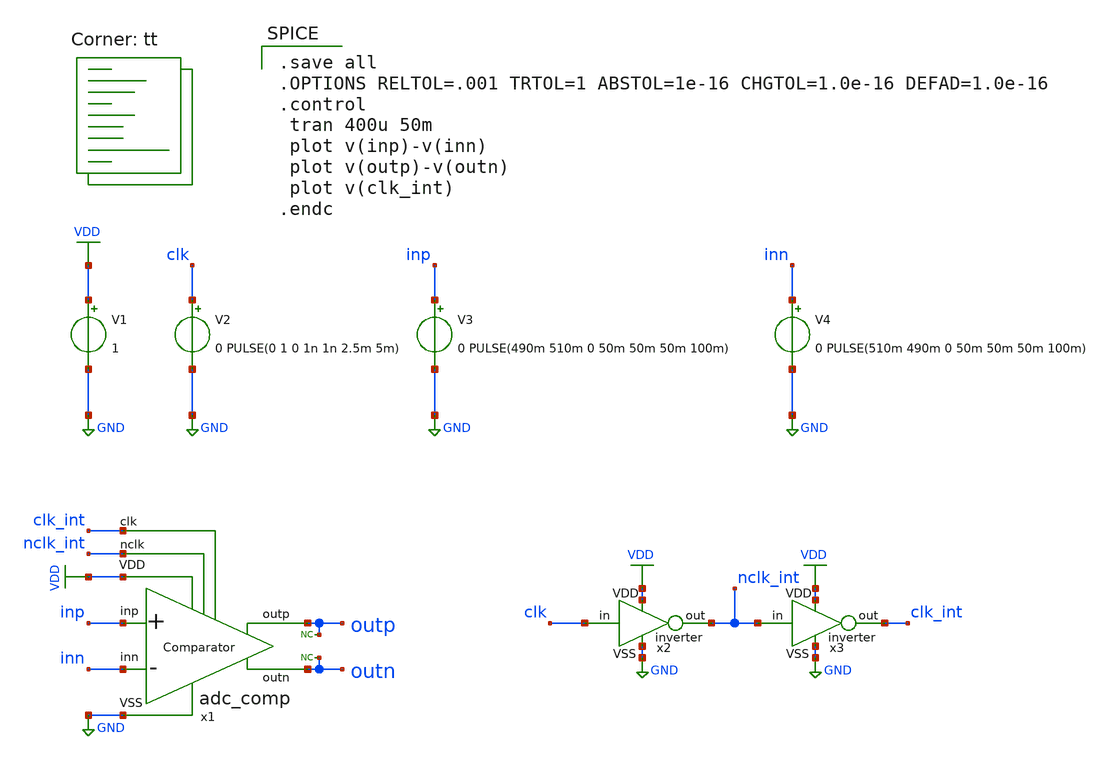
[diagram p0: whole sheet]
** sch_path: xschem/adc_comp/adc_comp_tb.sch
**.subckt adc_comp_tb
x1 VDD clk_int outp inp inn outn nclk_int GND adc_comp
V1 VDD GND 1
V2 clk GND 0 PULSE(0 1 0 1n 1n 2.5m 5m)
x2 VDD nclk_int clk GND inverter
x3 VDD clk_int nclk_int GND inverter
V3 inp GND 0 PULSE(490m 510m 0 50m 50m 50m 100m)
V4 inn GND 0 PULSE(510m 490m 0 50m 50m 50m 100m)
* noconn outp
* noconn outn
**** begin user architecture code
.lib $::SKYWATER_MODELS/sky130.lib.spice tt

.save all
.OPTIONS RELTOL=.001 TRTOL=1 ABSTOL=1e-16 CHGTOL=1.0e-16 DEFAD=1.0e-16
.control
 tran 400u 50m
 plot v(inp)-v(inn)
 plot v(outp)-v(outn)
 plot v(clk_int)
.endc

**** end user architecture code
**.ends
.GLOBAL GND
.GLOBAL VDD
.end
